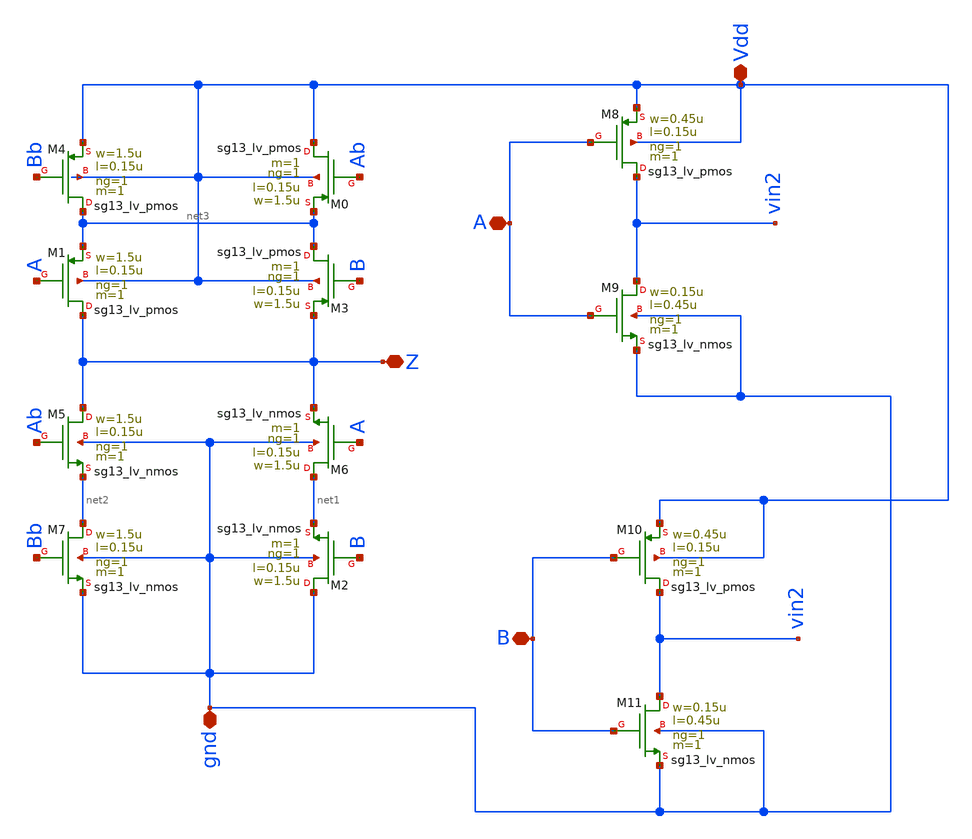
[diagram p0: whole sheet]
** sch_path: design/blocks/xor_ms/schematic/xor_ms.sch
**.subckt xor_ms Z Vdd A B gnd
*.iopin Z
*.iopin Vdd
*.iopin A
*.iopin B
*.iopin gnd
XM0 Vdd Ab net3 Vdd sg13_lv_pmos w=1.5u l=0.15u ng=1 m=1 mm_ok=1
XM2 gnd B net1 gnd sg13_lv_nmos w=1.5u l=0.15u ng=1 m=1 mm_ok=1
XM1 Z A net3 Vdd sg13_lv_pmos w=1.5u l=0.15u ng=1 m=1 mm_ok=1
XM3 net3 B Z Vdd sg13_lv_pmos w=1.5u l=0.15u ng=1 m=1 mm_ok=1
XM4 net3 Bb Vdd Vdd sg13_lv_pmos w=1.5u l=0.15u ng=1 m=1 mm_ok=1
XM5 Z Ab net2 gnd sg13_lv_nmos w=1.5u l=0.15u ng=1 m=1 mm_ok=1
XM6 net1 A Z gnd sg13_lv_nmos w=1.5u l=0.15u ng=1 m=1 mm_ok=1
XM7 net2 Bb gnd gnd sg13_lv_nmos w=1.5u l=0.15u ng=1 m=1 mm_ok=1
XM8 vin2 A Vdd Vdd sg13_lv_pmos w=0.45u l=0.15u ng=1 m=1 mm_ok=1
XM9 vin2 A gnd gnd sg13_lv_nmos w=0.15u l=0.45u ng=1 m=1 mm_ok=1
XM10 vin2 B Vdd Vdd sg13_lv_pmos w=0.45u l=0.15u ng=1 m=1 mm_ok=1
XM11 vin2 B gnd gnd sg13_lv_nmos w=0.15u l=0.45u ng=1 m=1 mm_ok=1
**.ends
.end
